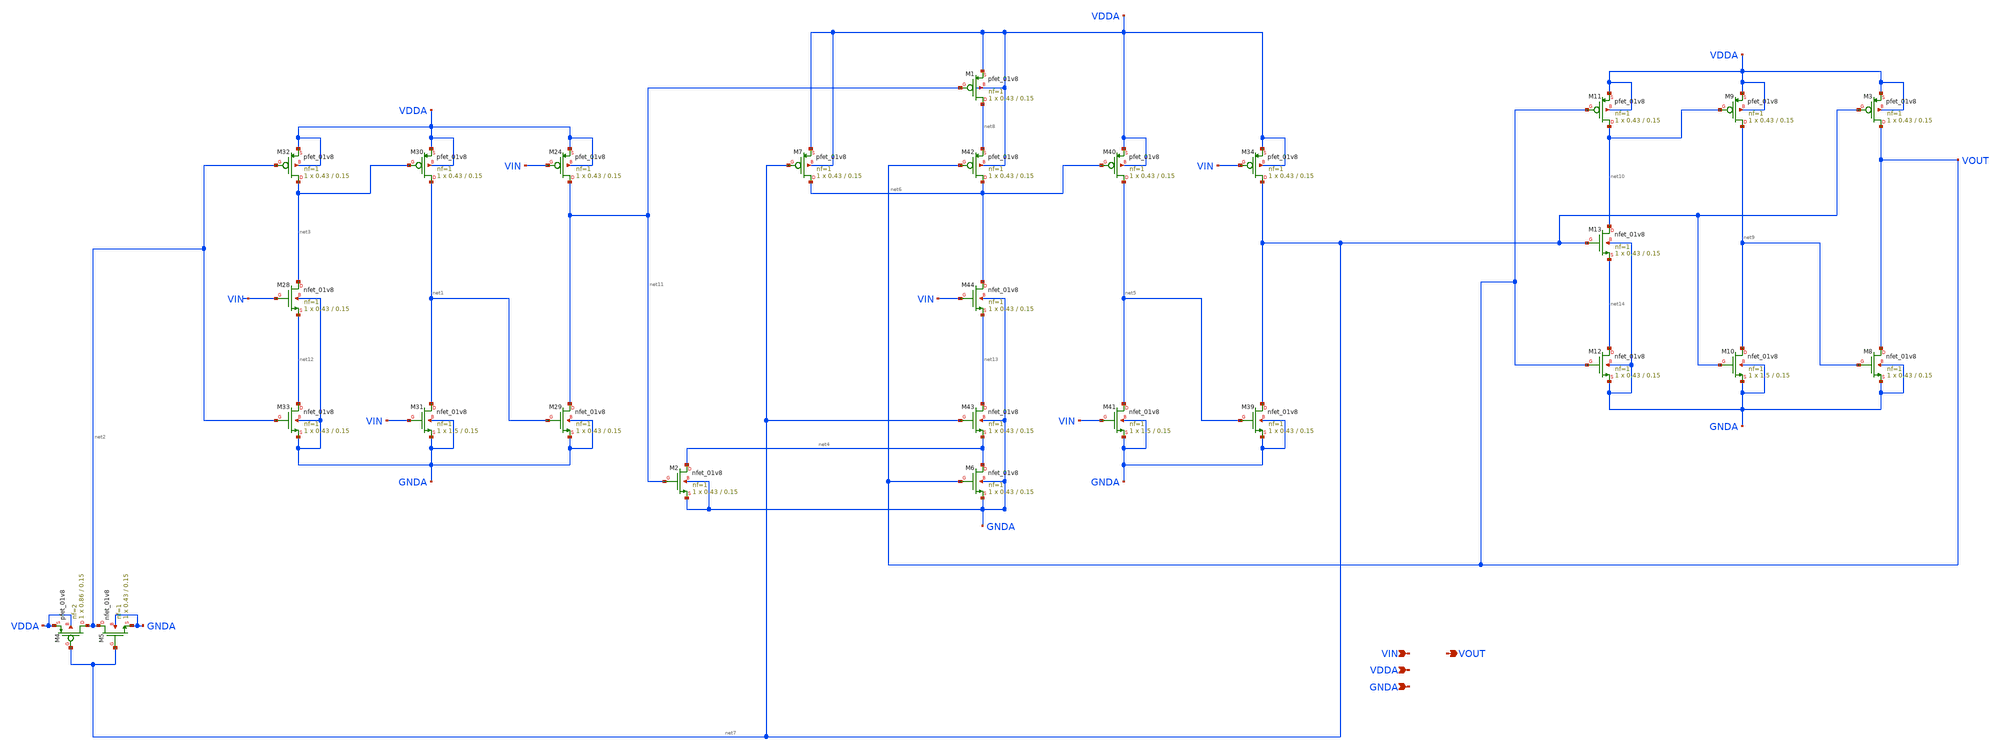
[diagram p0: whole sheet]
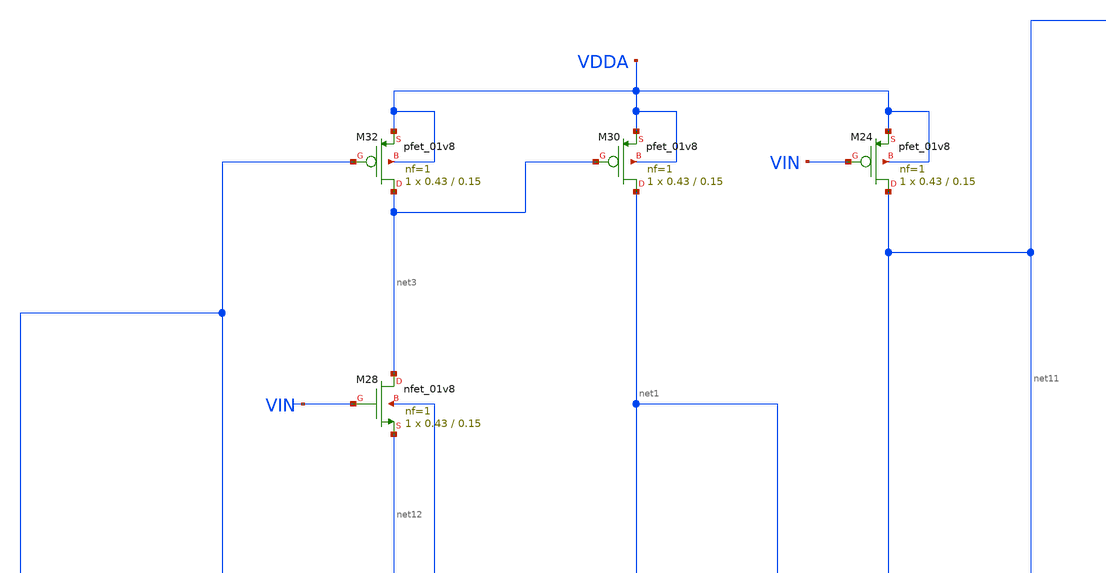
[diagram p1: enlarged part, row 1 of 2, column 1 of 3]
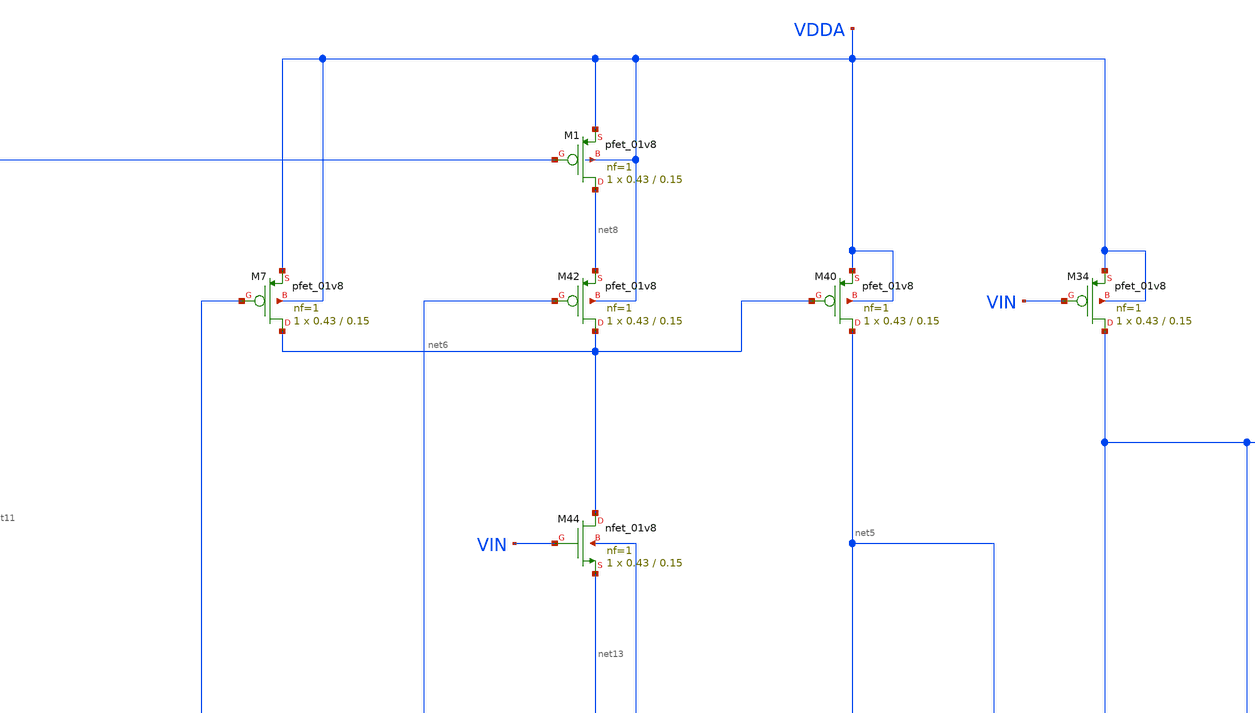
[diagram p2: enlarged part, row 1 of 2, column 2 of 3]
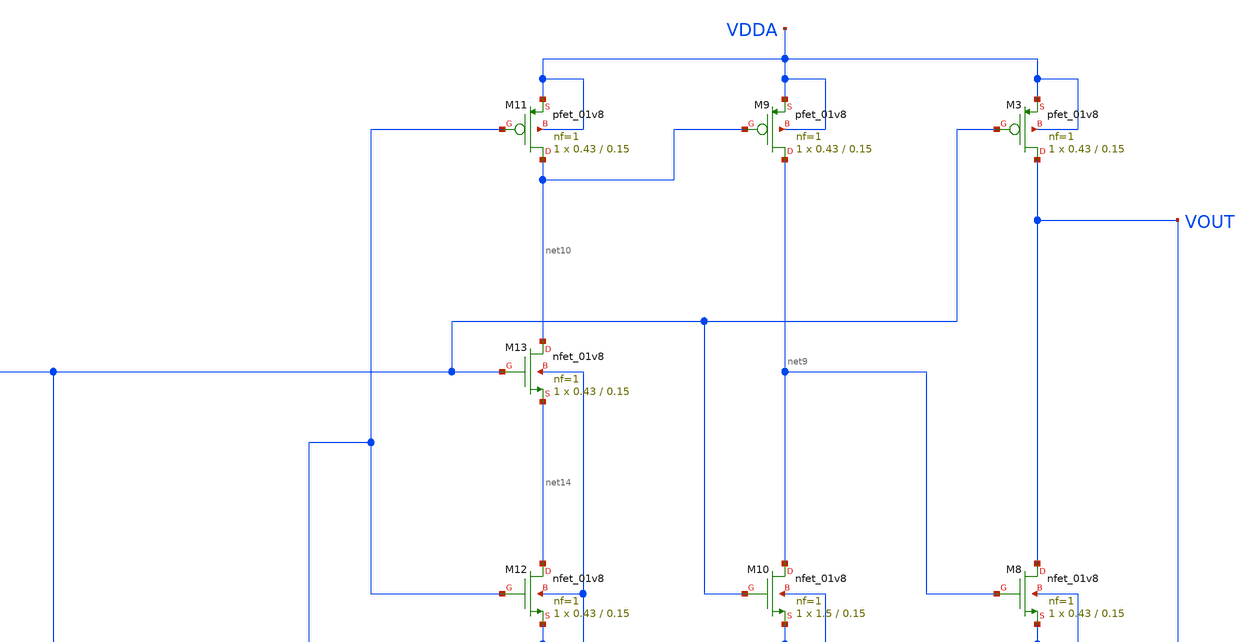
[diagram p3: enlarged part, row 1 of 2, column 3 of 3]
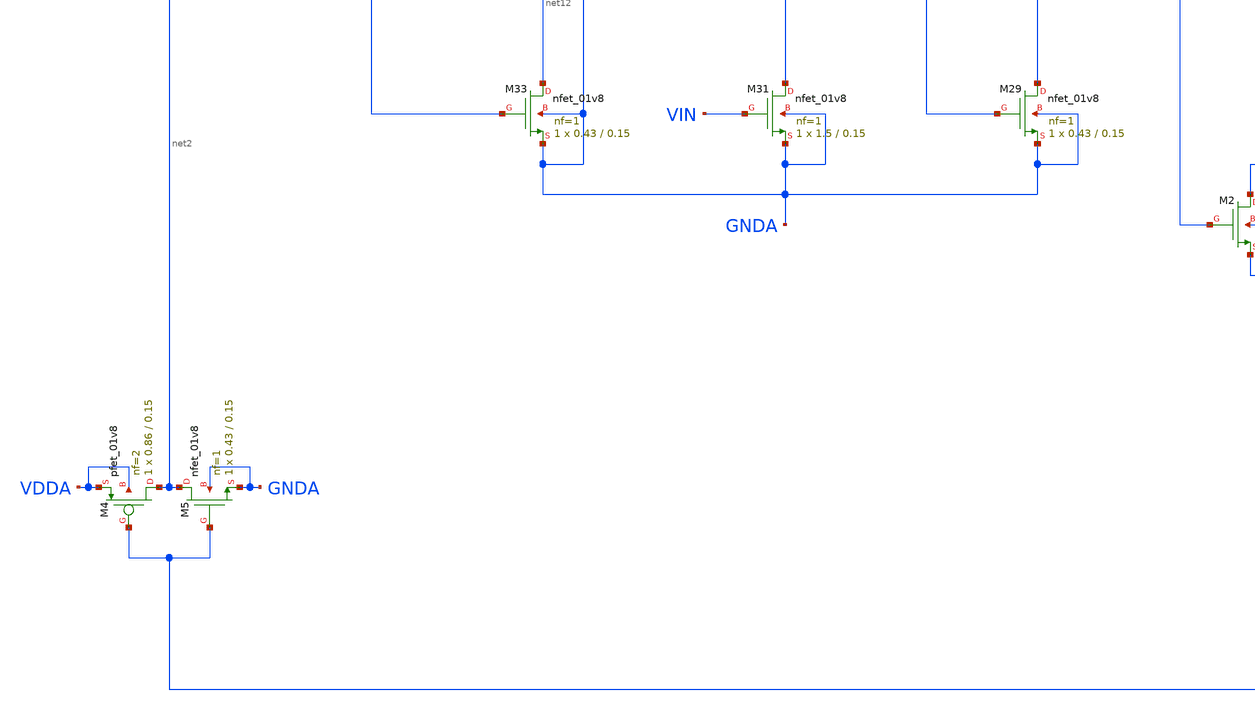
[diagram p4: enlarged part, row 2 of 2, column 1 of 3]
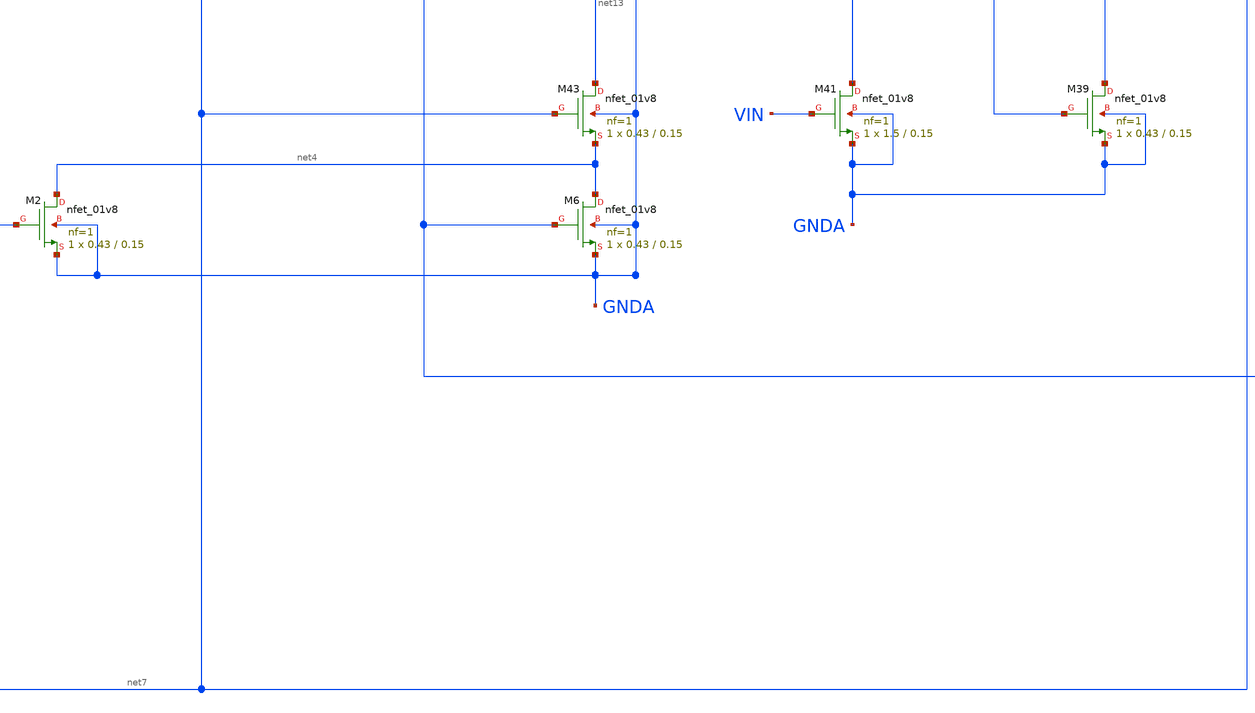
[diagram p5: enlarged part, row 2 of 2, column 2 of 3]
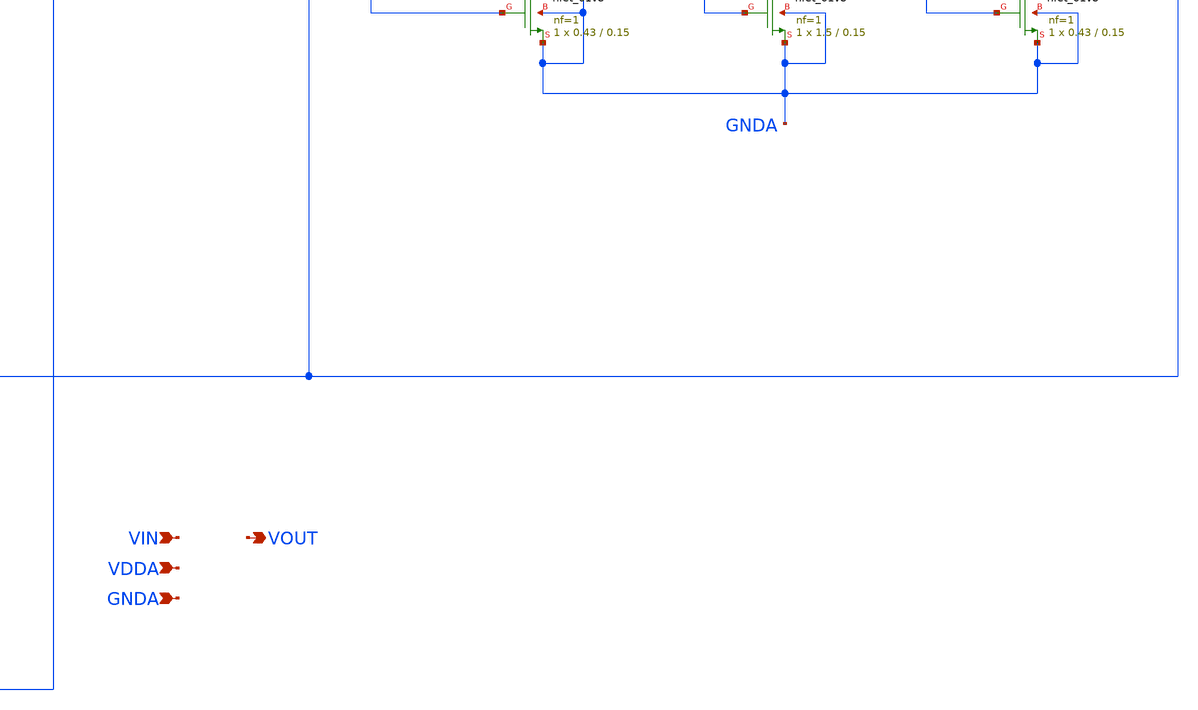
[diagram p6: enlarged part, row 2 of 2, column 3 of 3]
** sch_path: projects/pll/divider/xschem_ngspice/TSPC_FF_ratioed_divide5.sch
**.subckt TSPC_FF_ratioed_divide5 VIN VOUT VDDA GNDA
*.ipin VIN
*.opin VOUT
*.ipin VDDA
*.ipin GNDA
XM24 net11 VIN VDDA VDDA sky130_fd_pr__pfet_01v8 L=0.15 W=0.43 nf=1 ad='int((nf+1)/2) * W/nf * 0.29'
+ as='int((nf+2)/2) * W/nf * 0.29' pd='2*int((nf+1)/2) * (W/nf + 0.29)' ps='2*int((nf+2)/2) * (W/nf + 0.29)'
+ nrd='0.29 / W' nrs='0.29 / W' sa=0 sb=0 sd=0 mult=1 m=1
XM29 net11 net1 GNDA GNDA sky130_fd_pr__nfet_01v8 L=0.15 W=0.43 nf=1 ad='int((nf+1)/2) * W/nf * 0.29'
+ as='int((nf+2)/2) * W/nf * 0.29' pd='2*int((nf+1)/2) * (W/nf + 0.29)' ps='2*int((nf+2)/2) * (W/nf + 0.29)'
+ nrd='0.29 / W' nrs='0.29 / W' sa=0 sb=0 sd=0 mult=1 m=1
XM30 net1 net3 VDDA VDDA sky130_fd_pr__pfet_01v8 L=0.15 W=0.43 nf=1 ad='int((nf+1)/2) * W/nf * 0.29'
+ as='int((nf+2)/2) * W/nf * 0.29' pd='2*int((nf+1)/2) * (W/nf + 0.29)' ps='2*int((nf+2)/2) * (W/nf + 0.29)'
+ nrd='0.29 / W' nrs='0.29 / W' sa=0 sb=0 sd=0 mult=1 m=1
XM31 net1 VIN GNDA GNDA sky130_fd_pr__nfet_01v8 L=0.15 W=1.5 nf=1 ad='int((nf+1)/2) * W/nf * 0.29' as='int((nf+2)/2) * W/nf * 0.29'
+ pd='2*int((nf+1)/2) * (W/nf + 0.29)' ps='2*int((nf+2)/2) * (W/nf + 0.29)' nrd='0.29 / W' nrs='0.29 / W'
+ sa=0 sb=0 sd=0 mult=1 m=1
XM32 net3 net2 VDDA VDDA sky130_fd_pr__pfet_01v8 L=0.15 W=0.43 nf=1 ad='int((nf+1)/2) * W/nf * 0.29'
+ as='int((nf+2)/2) * W/nf * 0.29' pd='2*int((nf+1)/2) * (W/nf + 0.29)' ps='2*int((nf+2)/2) * (W/nf + 0.29)'
+ nrd='0.29 / W' nrs='0.29 / W' sa=0 sb=0 sd=0 mult=1 m=1
XM33 net12 net2 GNDA GNDA sky130_fd_pr__nfet_01v8 L=0.15 W=0.43 nf=1 ad='int((nf+1)/2) * W/nf * 0.29'
+ as='int((nf+2)/2) * W/nf * 0.29' pd='2*int((nf+1)/2) * (W/nf + 0.29)' ps='2*int((nf+2)/2) * (W/nf + 0.29)'
+ nrd='0.29 / W' nrs='0.29 / W' sa=0 sb=0 sd=0 mult=1 m=1
XM28 net3 VIN net12 GNDA sky130_fd_pr__nfet_01v8 L=0.15 W=0.43 nf=1 ad='int((nf+1)/2) * W/nf * 0.29'
+ as='int((nf+2)/2) * W/nf * 0.29' pd='2*int((nf+1)/2) * (W/nf + 0.29)' ps='2*int((nf+2)/2) * (W/nf + 0.29)'
+ nrd='0.29 / W' nrs='0.29 / W' sa=0 sb=0 sd=0 mult=1 m=1
XM34 net7 VIN VDDA VDDA sky130_fd_pr__pfet_01v8 L=0.15 W=0.43 nf=1 ad='int((nf+1)/2) * W/nf * 0.29' as='int((nf+2)/2) * W/nf * 0.29'
+ pd='2*int((nf+1)/2) * (W/nf + 0.29)' ps='2*int((nf+2)/2) * (W/nf + 0.29)' nrd='0.29 / W' nrs='0.29 / W'
+ sa=0 sb=0 sd=0 mult=1 m=1
XM39 net7 net5 GNDA GNDA sky130_fd_pr__nfet_01v8 L=0.15 W=0.43 nf=1 ad='int((nf+1)/2) * W/nf * 0.29'
+ as='int((nf+2)/2) * W/nf * 0.29' pd='2*int((nf+1)/2) * (W/nf + 0.29)' ps='2*int((nf+2)/2) * (W/nf + 0.29)'
+ nrd='0.29 / W' nrs='0.29 / W' sa=0 sb=0 sd=0 mult=1 m=1
XM40 net5 net6 VDDA VDDA sky130_fd_pr__pfet_01v8 L=0.15 W=0.43 nf=1 ad='int((nf+1)/2) * W/nf * 0.29'
+ as='int((nf+2)/2) * W/nf * 0.29' pd='2*int((nf+1)/2) * (W/nf + 0.29)' ps='2*int((nf+2)/2) * (W/nf + 0.29)'
+ nrd='0.29 / W' nrs='0.29 / W' sa=0 sb=0 sd=0 mult=1 m=1
XM41 net5 VIN GNDA GNDA sky130_fd_pr__nfet_01v8 L=0.15 W=1.5 nf=1 ad='int((nf+1)/2) * W/nf * 0.29' as='int((nf+2)/2) * W/nf * 0.29'
+ pd='2*int((nf+1)/2) * (W/nf + 0.29)' ps='2*int((nf+2)/2) * (W/nf + 0.29)' nrd='0.29 / W' nrs='0.29 / W'
+ sa=0 sb=0 sd=0 mult=1 m=1
XM42 net6 VOUT net8 VDDA sky130_fd_pr__pfet_01v8 L=0.15 W=0.43 nf=1 ad='int((nf+1)/2) * W/nf * 0.29'
+ as='int((nf+2)/2) * W/nf * 0.29' pd='2*int((nf+1)/2) * (W/nf + 0.29)' ps='2*int((nf+2)/2) * (W/nf + 0.29)'
+ nrd='0.29 / W' nrs='0.29 / W' sa=0 sb=0 sd=0 mult=1 m=1
XM43 net13 net7 net4 GNDA sky130_fd_pr__nfet_01v8 L=0.15 W=0.43 nf=1 ad='int((nf+1)/2) * W/nf * 0.29'
+ as='int((nf+2)/2) * W/nf * 0.29' pd='2*int((nf+1)/2) * (W/nf + 0.29)' ps='2*int((nf+2)/2) * (W/nf + 0.29)'
+ nrd='0.29 / W' nrs='0.29 / W' sa=0 sb=0 sd=0 mult=1 m=1
XM44 net6 VIN net13 GNDA sky130_fd_pr__nfet_01v8 L=0.15 W=0.43 nf=1 ad='int((nf+1)/2) * W/nf * 0.29'
+ as='int((nf+2)/2) * W/nf * 0.29' pd='2*int((nf+1)/2) * (W/nf + 0.29)' ps='2*int((nf+2)/2) * (W/nf + 0.29)'
+ nrd='0.29 / W' nrs='0.29 / W' sa=0 sb=0 sd=0 mult=1 m=1
XM4 net2 net7 VDDA VDDA sky130_fd_pr__pfet_01v8 L=0.15 W=0.86 nf=2 ad='int((nf+1)/2) * W/nf * 0.29' as='int((nf+2)/2) * W/nf * 0.29'
+ pd='2*int((nf+1)/2) * (W/nf + 0.29)' ps='2*int((nf+2)/2) * (W/nf + 0.29)' nrd='0.29 / W' nrs='0.29 / W'
+ sa=0 sb=0 sd=0 mult=1 m=1
XM5 net2 net7 GNDA GNDA sky130_fd_pr__nfet_01v8 L=0.15 W=0.43 nf=1 ad='int((nf+1)/2) * W/nf * 0.29' as='int((nf+2)/2) * W/nf * 0.29'
+ pd='2*int((nf+1)/2) * (W/nf + 0.29)' ps='2*int((nf+2)/2) * (W/nf + 0.29)' nrd='0.29 / W' nrs='0.29 / W'
+ sa=0 sb=0 sd=0 mult=1 m=1
XM6 net4 VOUT GNDA GNDA sky130_fd_pr__nfet_01v8 L=0.15 W=0.43 nf=1 ad='int((nf+1)/2) * W/nf * 0.29' as='int((nf+2)/2) * W/nf * 0.29'
+ pd='2*int((nf+1)/2) * (W/nf + 0.29)' ps='2*int((nf+2)/2) * (W/nf + 0.29)' nrd='0.29 / W' nrs='0.29 / W'
+ sa=0 sb=0 sd=0 mult=1 m=1
XM7 net6 net7 VDDA VDDA sky130_fd_pr__pfet_01v8 L=0.15 W=0.43 nf=1 ad='int((nf+1)/2) * W/nf * 0.29' as='int((nf+2)/2) * W/nf * 0.29'
+ pd='2*int((nf+1)/2) * (W/nf + 0.29)' ps='2*int((nf+2)/2) * (W/nf + 0.29)' nrd='0.29 / W' nrs='0.29 / W'
+ sa=0 sb=0 sd=0 mult=1 m=1
XM1 net8 net11 VDDA VDDA sky130_fd_pr__pfet_01v8 L=0.15 W=0.43 nf=1 ad='int((nf+1)/2) * W/nf * 0.29'
+ as='int((nf+2)/2) * W/nf * 0.29' pd='2*int((nf+1)/2) * (W/nf + 0.29)' ps='2*int((nf+2)/2) * (W/nf + 0.29)'
+ nrd='0.29 / W' nrs='0.29 / W' sa=0 sb=0 sd=0 mult=1 m=1
XM2 net4 net11 GNDA GNDA sky130_fd_pr__nfet_01v8 L=0.15 W=0.43 nf=1 ad='int((nf+1)/2) * W/nf * 0.29'
+ as='int((nf+2)/2) * W/nf * 0.29' pd='2*int((nf+1)/2) * (W/nf + 0.29)' ps='2*int((nf+2)/2) * (W/nf + 0.29)'
+ nrd='0.29 / W' nrs='0.29 / W' sa=0 sb=0 sd=0 mult=1 m=1
XM3 VOUT net7 VDDA VDDA sky130_fd_pr__pfet_01v8 L=0.15 W=0.43 nf=1 ad='int((nf+1)/2) * W/nf * 0.29' as='int((nf+2)/2) * W/nf * 0.29'
+ pd='2*int((nf+1)/2) * (W/nf + 0.29)' ps='2*int((nf+2)/2) * (W/nf + 0.29)' nrd='0.29 / W' nrs='0.29 / W'
+ sa=0 sb=0 sd=0 mult=1 m=1
XM8 VOUT net9 GNDA GNDA sky130_fd_pr__nfet_01v8 L=0.15 W=0.43 nf=1 ad='int((nf+1)/2) * W/nf * 0.29' as='int((nf+2)/2) * W/nf * 0.29'
+ pd='2*int((nf+1)/2) * (W/nf + 0.29)' ps='2*int((nf+2)/2) * (W/nf + 0.29)' nrd='0.29 / W' nrs='0.29 / W'
+ sa=0 sb=0 sd=0 mult=1 m=1
XM9 net9 net10 VDDA VDDA sky130_fd_pr__pfet_01v8 L=0.15 W=0.43 nf=1 ad='int((nf+1)/2) * W/nf * 0.29'
+ as='int((nf+2)/2) * W/nf * 0.29' pd='2*int((nf+1)/2) * (W/nf + 0.29)' ps='2*int((nf+2)/2) * (W/nf + 0.29)'
+ nrd='0.29 / W' nrs='0.29 / W' sa=0 sb=0 sd=0 mult=1 m=1
XM10 net9 net7 GNDA GNDA sky130_fd_pr__nfet_01v8 L=0.15 W=1.5 nf=1 ad='int((nf+1)/2) * W/nf * 0.29' as='int((nf+2)/2) * W/nf * 0.29'
+ pd='2*int((nf+1)/2) * (W/nf + 0.29)' ps='2*int((nf+2)/2) * (W/nf + 0.29)' nrd='0.29 / W' nrs='0.29 / W'
+ sa=0 sb=0 sd=0 mult=1 m=1
XM11 net10 VOUT VDDA VDDA sky130_fd_pr__pfet_01v8 L=0.15 W=0.43 nf=1 ad='int((nf+1)/2) * W/nf * 0.29'
+ as='int((nf+2)/2) * W/nf * 0.29' pd='2*int((nf+1)/2) * (W/nf + 0.29)' ps='2*int((nf+2)/2) * (W/nf + 0.29)'
+ nrd='0.29 / W' nrs='0.29 / W' sa=0 sb=0 sd=0 mult=1 m=1
XM12 net14 VOUT GNDA GNDA sky130_fd_pr__nfet_01v8 L=0.15 W=0.43 nf=1 ad='int((nf+1)/2) * W/nf * 0.29'
+ as='int((nf+2)/2) * W/nf * 0.29' pd='2*int((nf+1)/2) * (W/nf + 0.29)' ps='2*int((nf+2)/2) * (W/nf + 0.29)'
+ nrd='0.29 / W' nrs='0.29 / W' sa=0 sb=0 sd=0 mult=1 m=1
XM13 net10 net7 net14 GNDA sky130_fd_pr__nfet_01v8 L=0.15 W=0.43 nf=1 ad='int((nf+1)/2) * W/nf * 0.29'
+ as='int((nf+2)/2) * W/nf * 0.29' pd='2*int((nf+1)/2) * (W/nf + 0.29)' ps='2*int((nf+2)/2) * (W/nf + 0.29)'
+ nrd='0.29 / W' nrs='0.29 / W' sa=0 sb=0 sd=0 mult=1 m=1
**.ends
.end
